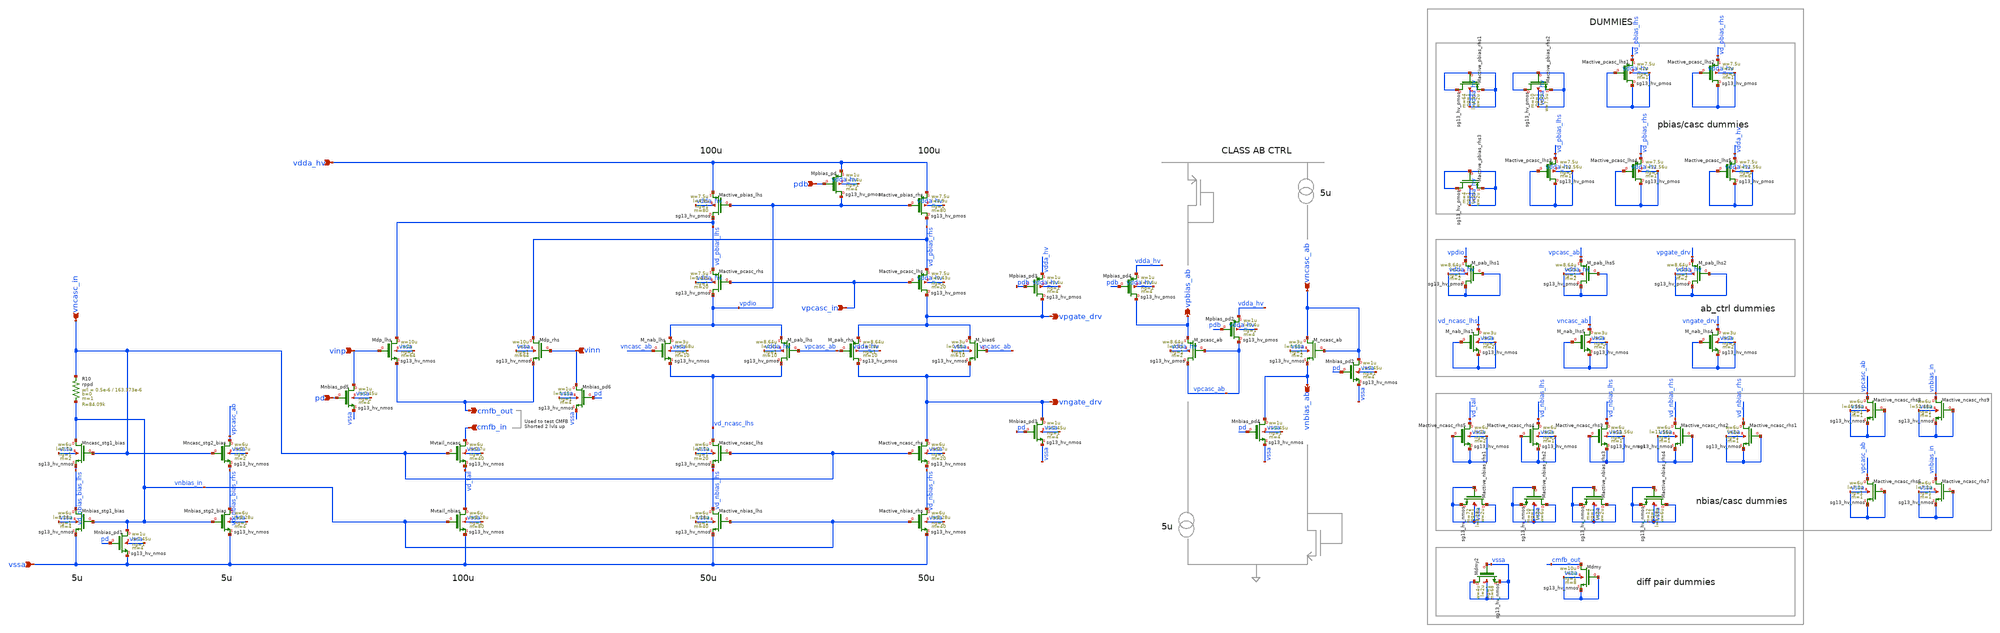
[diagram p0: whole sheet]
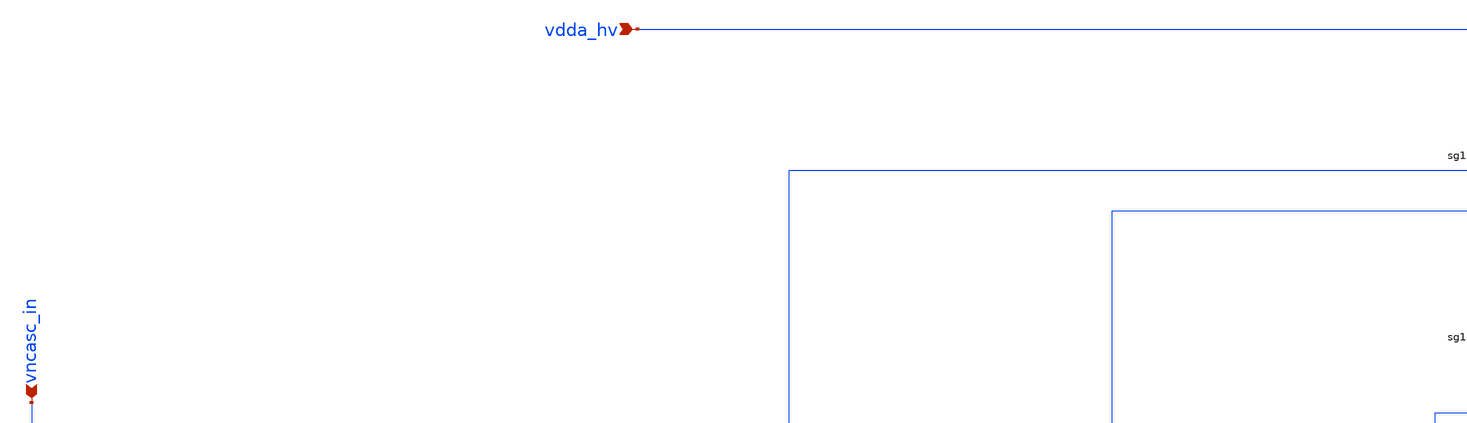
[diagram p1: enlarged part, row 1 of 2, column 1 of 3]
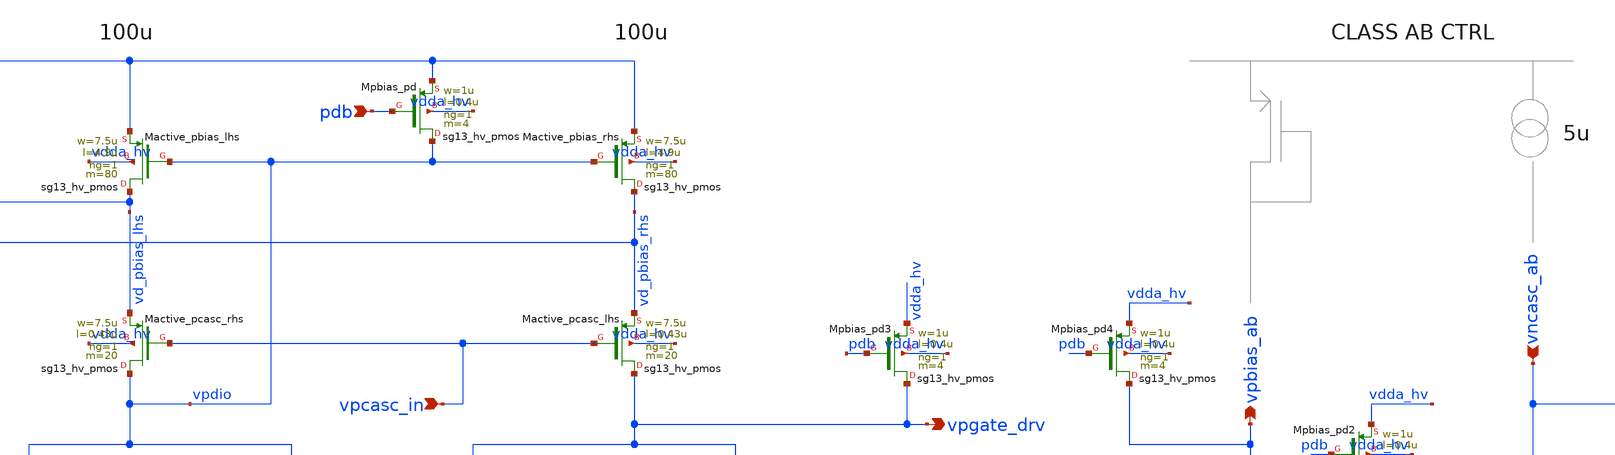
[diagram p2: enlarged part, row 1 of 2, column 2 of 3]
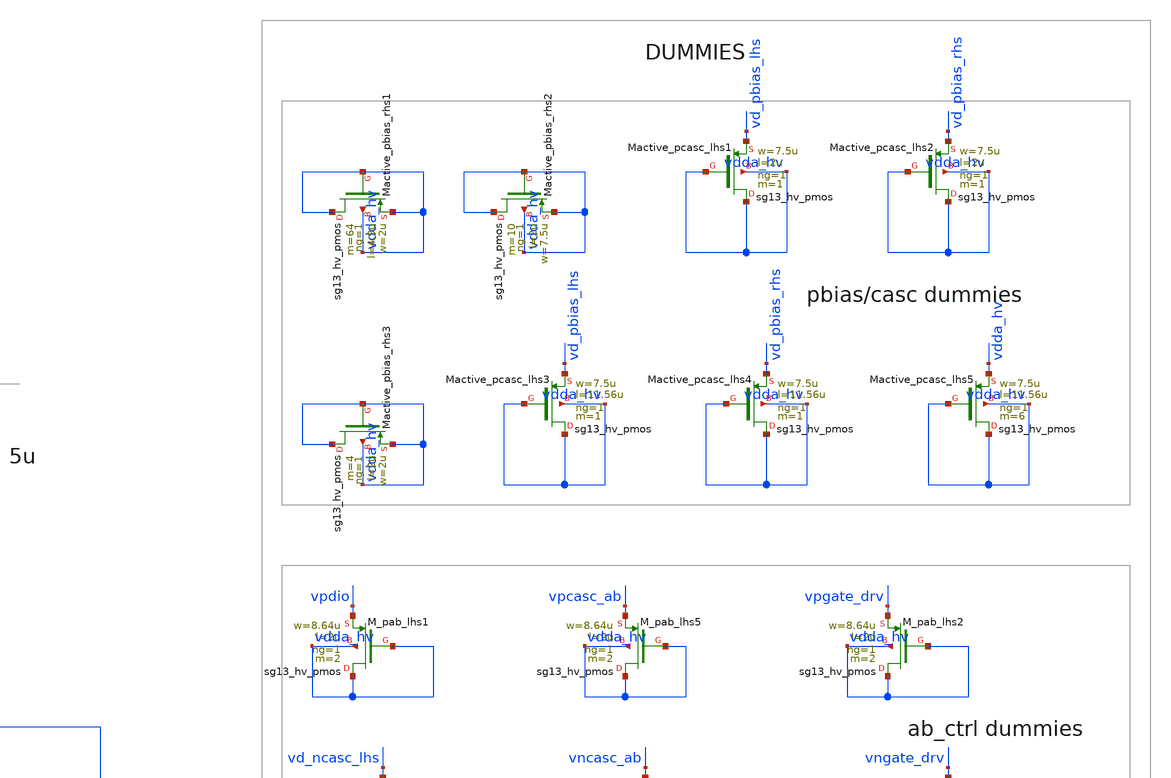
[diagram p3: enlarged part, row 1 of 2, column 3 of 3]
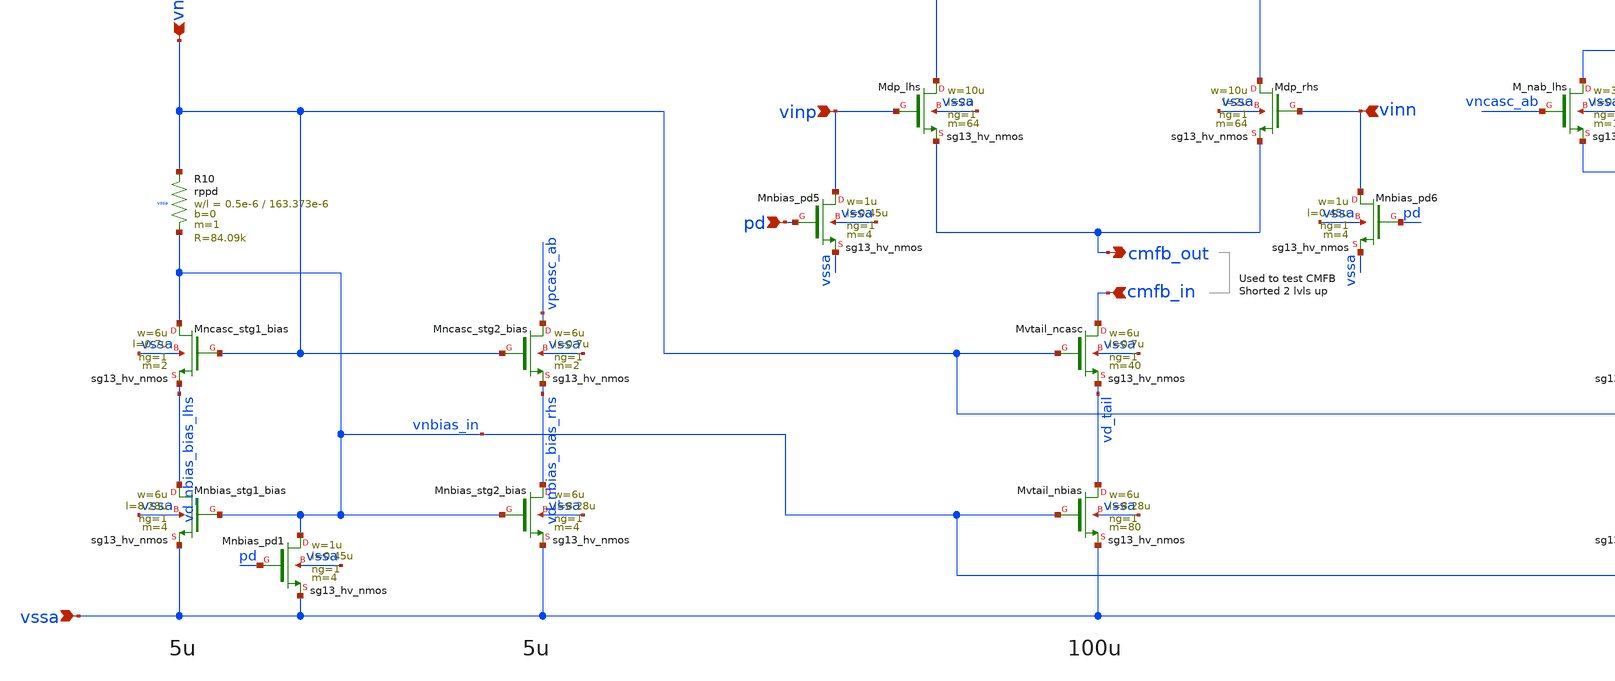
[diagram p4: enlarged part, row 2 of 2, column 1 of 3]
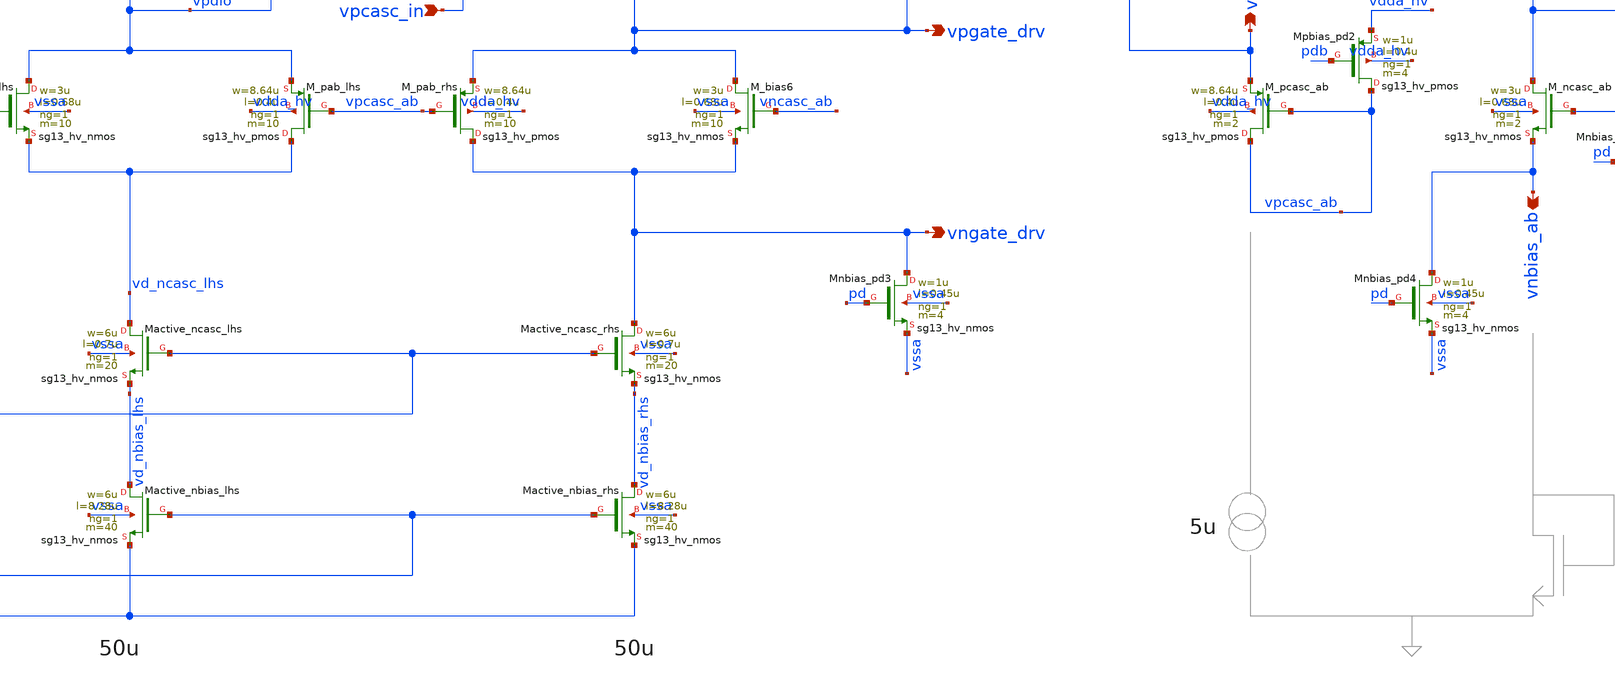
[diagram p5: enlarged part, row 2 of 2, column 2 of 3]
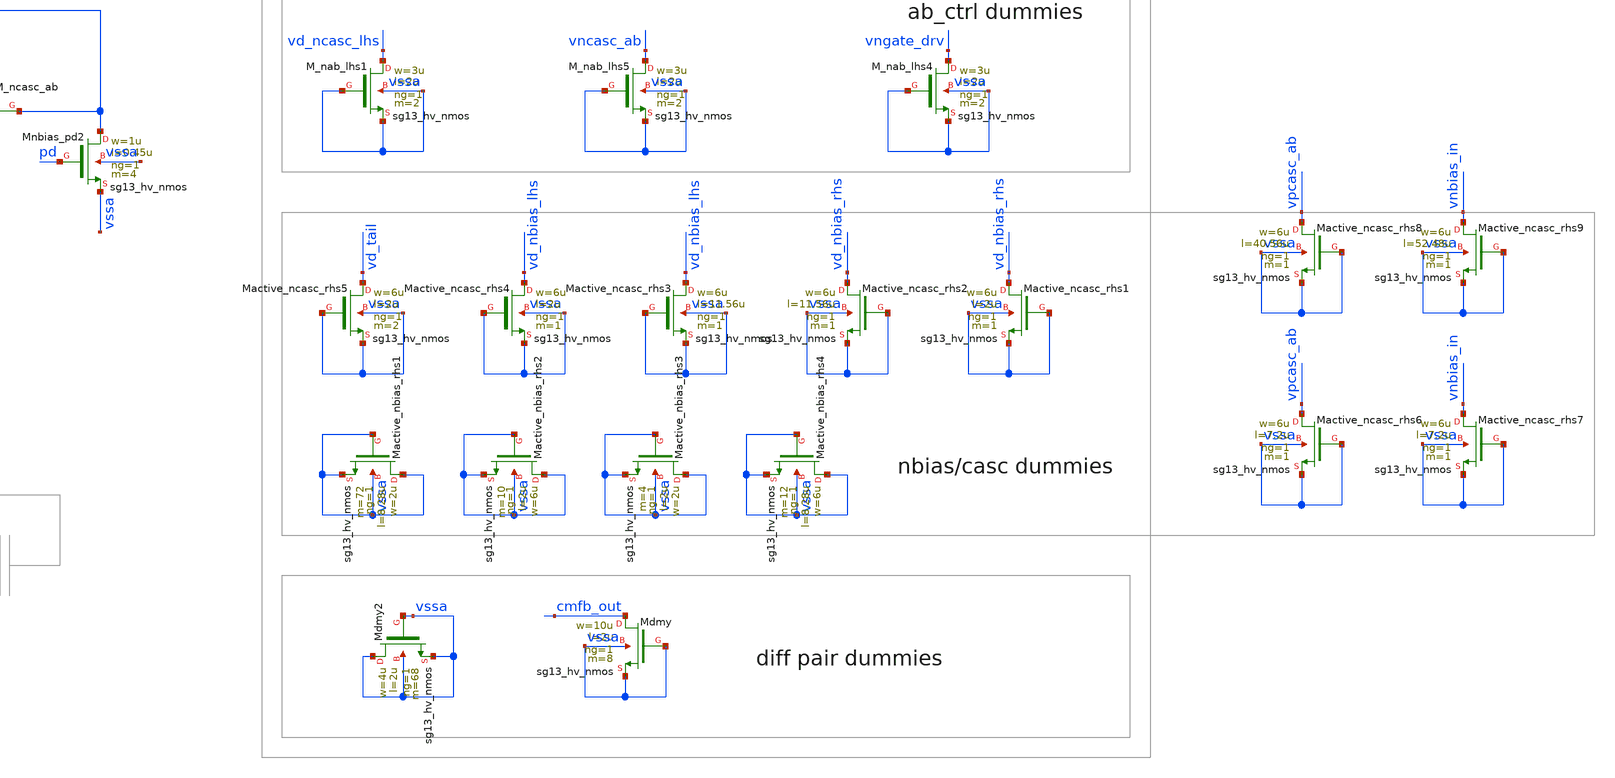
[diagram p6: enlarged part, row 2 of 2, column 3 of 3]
** sch_path: Schematics_Layout/sunrise_opamp_stg1/sunrise_opamp_stg1.sch
**.subckt sunrise_opamp_stg1 vinp vinn pdb pd vdda_hv vpcasc_in vpgate_drv vngate_drv cmfb_in
*+ cmfb_out vncasc_ab vncasc_in vssa vnbias_ab vpbias_ab
*.ipin vinp
*.ipin vinn
*.ipin pdb
*.ipin pd
*.ipin vdda_hv
*.ipin vpcasc_in
*.opin vpgate_drv
*.opin vngate_drv
*.ipin cmfb_in
*.opin cmfb_out
*.ipin vncasc_ab
*.ipin vncasc_in
*.ipin vssa
*.opin vnbias_ab
*.opin vpbias_ab
XMactive_nbias_rhs vd_nbias_rhs vnbias_in vssa vssa sg13_hv_nmos w=6u l=8.28u ng=1 m=40 mm_ok=1
XMactive_ncasc_rhs vngate_drv vncasc_in vd_nbias_rhs vssa sg13_hv_nmos w=6u l=0.7u ng=1 m=20 mm_ok=1
XMactive_nbias_lhs vd_nbias_lhs vnbias_in vssa vssa sg13_hv_nmos w=6u l=8.28u ng=1 m=40 mm_ok=1
XMactive_ncasc_lhs vd_ncasc_lhs vncasc_in vd_nbias_lhs vssa sg13_hv_nmos w=6u l=0.7u ng=1 m=20
+ mm_ok=1
XMactive_pcasc_lhs vpgate_drv vpcasc_in vd_pbias_rhs vdda_hv sg13_hv_pmos w=7.5u l=0.43u ng=1 m=20
+ mm_ok=1
XMactive_pbias_rhs vd_pbias_rhs vpdio vdda_hv vdda_hv sg13_hv_pmos w=7.5u l=4.9u ng=1 m=80 mm_ok=1
XMactive_pcasc_rhs vpdio vpcasc_in vd_pbias_lhs vdda_hv sg13_hv_pmos w=7.5u l=0.43u ng=1 m=20
+ mm_ok=1
XMactive_pbias_lhs vd_pbias_lhs vpdio vdda_hv vdda_hv sg13_hv_pmos w=7.5u l=4.9u ng=1 m=80 mm_ok=1
XMdp_lhs vd_pbias_lhs vinp cmfb_out vssa sg13_hv_nmos w=10u l=2u ng=1 m=64 mm_ok=1
XMdp_rhs vd_pbias_rhs vinn cmfb_out vssa sg13_hv_nmos w=10u l=2u ng=1 m=64 mm_ok=1
XMvtail_nbias vd_tail vnbias_in vssa vssa sg13_hv_nmos w=6u l=8.28u ng=1 m=80 mm_ok=1
XMvtail_ncasc cmfb_in vncasc_in vd_tail vssa sg13_hv_nmos w=6u l=0.7u ng=1 m=40 mm_ok=1
XM_bias6 vpgate_drv vncasc_ab vngate_drv vssa sg13_hv_nmos w=3u l=0.68u ng=1 m=10 mm_ok=1
XM_pab_rhs vngate_drv vpcasc_ab vpgate_drv vdda_hv sg13_hv_pmos w=8.64u l=0.4u ng=1 m=10 mm_ok=1
XM_nab_lhs vpdio vncasc_ab vd_ncasc_lhs vssa sg13_hv_nmos w=3u l=0.68u ng=1 m=10 mm_ok=1
XM_pab_lhs vd_ncasc_lhs vpcasc_ab vpdio vdda_hv sg13_hv_pmos w=8.64u l=0.4u ng=1 m=10 mm_ok=1
XMpbias_pd vpdio pdb vdda_hv vdda_hv sg13_hv_pmos w=1u l=0.4u ng=1 m=4 mm_ok=1
XMnbias_pd5 vinp pd vssa vssa sg13_hv_nmos w=1u l=0.45u ng=1 m=4 mm_ok=1
XMnbias_pd6 vinn pd vssa vssa sg13_hv_nmos w=1u l=0.45u ng=1 m=4 mm_ok=1
XMdmy2 vssa vssa vssa vssa sg13_hv_nmos w=4u l=2u ng=1 m=68 mm_ok=1
XMdmy cmfb_out vssa vssa vssa sg13_hv_nmos w=10u l=2u ng=1 m=8 mm_ok=1
XMactive_nbias_rhs1 vssa vssa vssa vssa sg13_hv_nmos w=2u l=8.28u ng=1 m=72 mm_ok=1
XMactive_nbias_rhs2 vssa vssa vssa vssa sg13_hv_nmos w=6u l=2u ng=1 m=10 mm_ok=1
XMactive_nbias_rhs3 vssa vssa vssa vssa sg13_hv_nmos w=2u l=2u ng=1 m=4 mm_ok=1
XMactive_nbias_rhs4 vssa vssa vssa vssa sg13_hv_nmos w=6u l=8.28u ng=1 m=12 mm_ok=1
XMactive_ncasc_rhs1 vd_nbias_rhs vssa vssa vssa sg13_hv_nmos w=6u l=2u ng=1 m=1 mm_ok=1
XMactive_ncasc_rhs2 vd_nbias_rhs vssa vssa vssa sg13_hv_nmos w=6u l=11.56u ng=1 m=1 mm_ok=1
XMactive_ncasc_rhs3 vd_nbias_lhs vssa vssa vssa sg13_hv_nmos w=6u l=11.56u ng=1 m=1 mm_ok=1
XMactive_ncasc_rhs4 vd_nbias_lhs vssa vssa vssa sg13_hv_nmos w=6u l=2u ng=1 m=1 mm_ok=1
XMactive_ncasc_rhs5 vd_tail vssa vssa vssa sg13_hv_nmos w=6u l=2u ng=1 m=2 mm_ok=1
XMactive_pbias_rhs1 vdda_hv vdda_hv vdda_hv vdda_hv sg13_hv_pmos w=2u l=4.9u ng=1 m=64 mm_ok=1
XMactive_pbias_rhs2 vdda_hv vdda_hv vdda_hv vdda_hv sg13_hv_pmos w=7.5u l=2u ng=1 m=10 mm_ok=1
XMactive_pbias_rhs3 vdda_hv vdda_hv vdda_hv vdda_hv sg13_hv_pmos w=2u l=2u ng=1 m=4 mm_ok=1
XMactive_pcasc_lhs1 vdda_hv vdda_hv vd_pbias_lhs vdda_hv sg13_hv_pmos w=7.5u l=2u ng=1 m=1 mm_ok=1
XMactive_pcasc_lhs2 vdda_hv vdda_hv vd_pbias_rhs vdda_hv sg13_hv_pmos w=7.5u l=2u ng=1 m=1 mm_ok=1
XMactive_pcasc_lhs3 vdda_hv vdda_hv vd_pbias_lhs vdda_hv sg13_hv_pmos w=7.5u l=11.56u ng=1 m=1
+ mm_ok=1
XMactive_pcasc_lhs4 vdda_hv vdda_hv vd_pbias_rhs vdda_hv sg13_hv_pmos w=7.5u l=11.56u ng=1 m=1
+ mm_ok=1
XMactive_pcasc_lhs5 vdda_hv vdda_hv vdda_hv vdda_hv sg13_hv_pmos w=7.5u l=11.56u ng=1 m=6 mm_ok=1
XM_pab_lhs1 vdda_hv vdda_hv vpdio vdda_hv sg13_hv_pmos w=8.64u l=2u ng=1 m=2 mm_ok=1
XM_pab_lhs2 vdda_hv vdda_hv vpgate_drv vdda_hv sg13_hv_pmos w=8.64u l=2u ng=1 m=2 mm_ok=1
XM_nab_lhs1 vd_ncasc_lhs vssa vssa vssa sg13_hv_nmos w=3u l=2u ng=1 m=2 mm_ok=1
XM_nab_lhs4 vngate_drv vssa vssa vssa sg13_hv_nmos w=3u l=2u ng=1 m=2 mm_ok=1
XMnbias_stg1_bias vd_nbias_bias_lhs vnbias_in vssa vssa sg13_hv_nmos w=6u l=8.28u ng=1 m=4 mm_ok=1
XMncasc_stg1_bias vnbias_in vncasc_in vd_nbias_bias_lhs vssa sg13_hv_nmos w=6u l=0.7u ng=1 m=2
+ mm_ok=1
XMnbias_stg2_bias vd_nbias_bias_rhs vnbias_in vssa vssa sg13_hv_nmos w=6u l=8.28u ng=1 m=4 mm_ok=1
XMncasc_stg2_bias vpcasc_ab vncasc_in vd_nbias_bias_rhs vssa sg13_hv_nmos w=6u l=0.7u ng=1 m=2
+ mm_ok=1
XM_pcasc_ab vpcasc_ab vpcasc_ab vpbias_ab vdda_hv sg13_hv_pmos w=8.64u l=0.4u ng=1 m=2 mm_ok=1
XM_ncasc_ab vncasc_ab vncasc_ab vnbias_ab vssa sg13_hv_nmos w=3u l=0.68u ng=1 m=2 mm_ok=1
XR10 vncasc_in vnbias_in vssa rppd w=0.5e-6 l=163.373e-6 m=1 b=0 mm_ok=1
XMnbias_pd1 vnbias_in pd vssa vssa sg13_hv_nmos w=1u l=0.45u ng=1 m=4 mm_ok=1
XMactive_ncasc_rhs6 vpcasc_ab vssa vssa vssa sg13_hv_nmos w=6u l=7.2u ng=1 m=1 mm_ok=1
XMactive_ncasc_rhs7 vnbias_in vssa vssa vssa sg13_hv_nmos w=6u l=7.2u ng=1 m=1 mm_ok=1
XMactive_ncasc_rhs8 vpcasc_ab vssa vssa vssa sg13_hv_nmos w=6u l=40.56u ng=1 m=1 mm_ok=1
XMactive_ncasc_rhs9 vnbias_in vssa vssa vssa sg13_hv_nmos w=6u l=52.48u ng=1 m=1 mm_ok=1
XM_nab_lhs5 vncasc_ab vssa vssa vssa sg13_hv_nmos w=3u l=2u ng=1 m=2 mm_ok=1
XM_pab_lhs5 vdda_hv vdda_hv vpcasc_ab vdda_hv sg13_hv_pmos w=8.64u l=2u ng=1 m=2 mm_ok=1
XMnbias_pd2 vncasc_ab pd vssa vssa sg13_hv_nmos w=1u l=0.45u ng=1 m=4 mm_ok=1
XMpbias_pd2 vpcasc_ab pdb vdda_hv vdda_hv sg13_hv_pmos w=1u l=0.4u ng=1 m=4 mm_ok=1
XMnbias_pd3 vngate_drv pd vssa vssa sg13_hv_nmos w=1u l=0.45u ng=1 m=4 mm_ok=1
XMnbias_pd4 vnbias_ab pd vssa vssa sg13_hv_nmos w=1u l=0.45u ng=1 m=4 mm_ok=1
XMpbias_pd3 vpgate_drv pdb vdda_hv vdda_hv sg13_hv_pmos w=1u l=0.4u ng=1 m=4 mm_ok=1
XMpbias_pd4 vpbias_ab pdb vdda_hv vdda_hv sg13_hv_pmos w=1u l=0.4u ng=1 m=4 mm_ok=1
**.ends
.end
